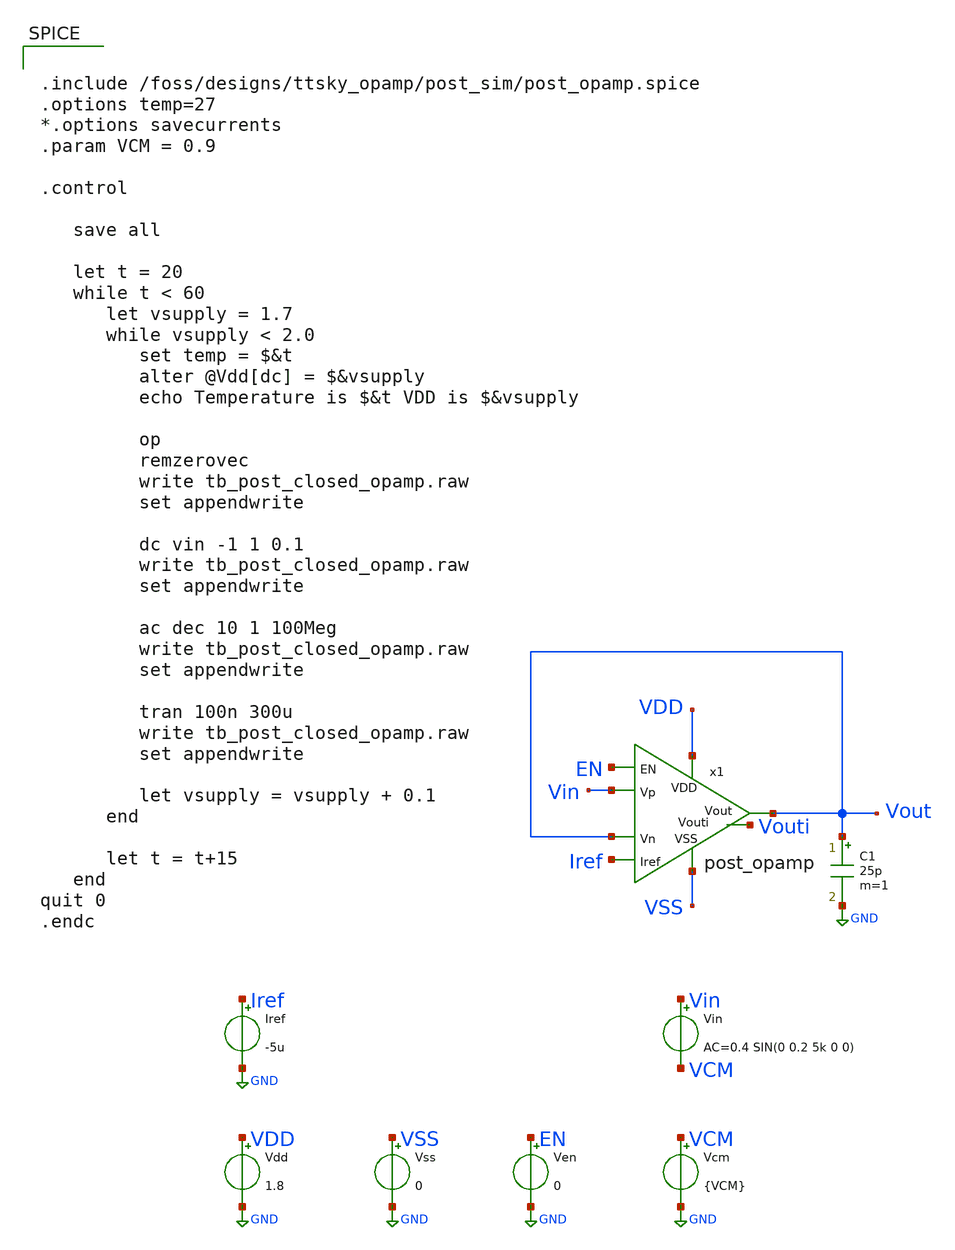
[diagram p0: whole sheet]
** sch_path: xschem/tb_post_closed_opamp.sch
**.subckt tb_post_closed_opamp
Vdd VDD GND 1.8
Vss VSS GND 0
Vin Vin VCM AC=0.4 SIN(0 0.2 5k 0 0)
Iref Iref GND -5u
Ven EN GND 0
C1 Vout GND 25p m=1
Vcm VCM GND {VCM}
x1 Vout Vout Vin VSS Iref VDD Vouti EN post_opamp
**** begin user architecture code


.include /foss/designs/ttsky_opamp/post_sim/post_opamp.spice
.options temp=27
*.options savecurrents
.param VCM = 0.9

.control

   save all

   let t = 20
   while t < 60
      let vsupply = 1.7
      while vsupply < 2.0
         set temp = $&t
         alter @Vdd[dc] = $&vsupply
         echo Temperature is $&t VDD is $&vsupply

         op
         remzerovec
         write tb_post_closed_opamp.raw
         set appendwrite

         dc vin -1 1 0.1
         write tb_post_closed_opamp.raw
         set appendwrite

         ac dec 10 1 100Meg
         write tb_post_closed_opamp.raw
         set appendwrite

         tran 100n 300u
         write tb_post_closed_opamp.raw
         set appendwrite

         let vsupply = vsupply + 0.1
      end

      let t = t+15
   end
quit 0
.endc



** opencircuitdesign pdks install
.param MT_SWITCH = 1.0
.lib $::SKYWATER_MODELS/sky130.lib.spice ff

**** end user architecture code
**.ends
.GLOBAL GND
.end
